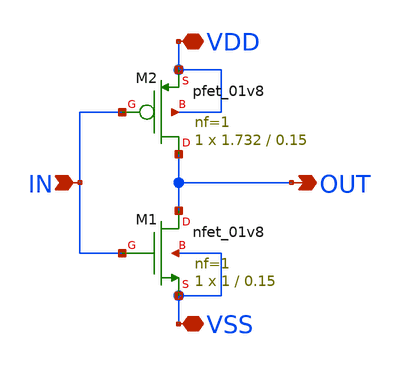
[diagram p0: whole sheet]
** sch_path: design/inv_with_fo4/inverter.sch
**.subckt inverter IN VDD OUT VSS
*.ipin IN
*.iopin VDD
*.opin OUT
*.iopin VSS
XM2 OUT IN VDD VDD sky130_fd_pr__pfet_01v8 L=0.15 W=1.732 nf=1 ad='int((nf+1)/2) * W/nf * 0.29' as='int((nf+2)/2) * W/nf * 0.29'
+ pd='2*int((nf+1)/2) * (W/nf + 0.29)' ps='2*int((nf+2)/2) * (W/nf + 0.29)' nrd='0.29 / W' nrs='0.29 / W'
+ sa=0 sb=0 sd=0 mult=1 m=1
XM1 OUT IN VSS VSS sky130_fd_pr__nfet_01v8 L=0.15 W=1 nf=1 ad='int((1 + 1)/2) * 1 / 1 * 0.29' as='int((1 + 2)/2) * 1 / 1 * 0.29'
+ pd='2*int((1 + 1)/2) * (1 / 1 + 0.29)' ps='2*int((1 + 2)/2) * (1 / 1 + 0.29)' nrd='0.29 / 1 ' nrs='0.29 / 1 '
+ sa=0 sb=0 sd=0 mult=1 m=1
**.ends
.end
